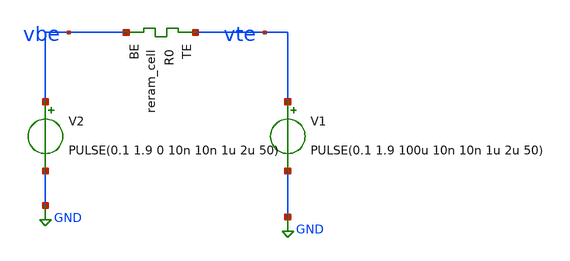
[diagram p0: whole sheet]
** sch_path: Synapse/synapsis.sch
**.subckt synapsis
XR0 vte vbe sky130_fd_pr_reram__reram_cell Tfilament_0=4.4e-9
V2 vbe GND PULSE(0.1 1.9 0 10n 10n 1u 2u 50)
V1 vte GND PULSE(0.1 1.9 100u 10n 10n 1u 2u 50)
**** begin user architecture code

** opencircuitdesign pdks install
.inc $::SKYWATER_MODELS/sky130_fd_pr_reram__reram_cell.spice



.options savecurrents
.control
save all
tran 10n 200u
write synapsis.raw
.endc



**** end user architecture code
**.ends
.GLOBAL GND
.end
